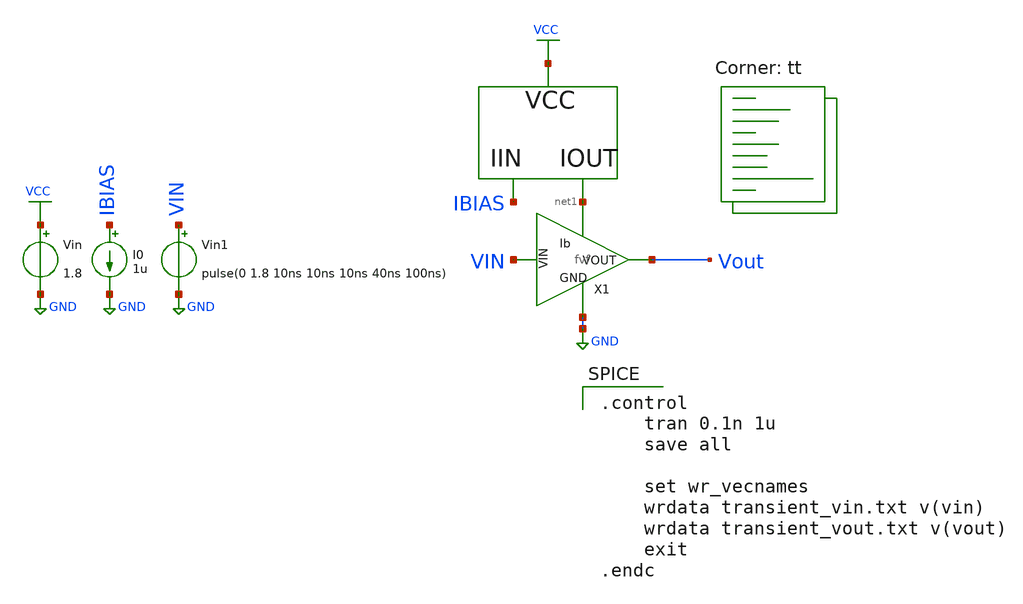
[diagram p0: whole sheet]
** sch_path: xschem/fvf_tb_tran.sch
**.subckt fvf_tb_tran
Vin VCC GND 1.8
I0 IBIAS GND 1u
X1 net1 GND VIN Vout fvf
Vin1 VIN GND pulse(0 1.8 10ns 10ns 10ns 40ns 100ns)
**** begin user architecture code
.lib $::SKYWATER_MODELS/sky130.lib.spice tt

.control
    tran 0.1n 1u
    save all

    set wr_vecnames
    wrdata transient_vin.txt v(vin)
    wrdata transient_vout.txt v(vout)
    exit
.endc

**** end user architecture code
**.ends

* expanding   symbol:  /foss/designs/fvf-chipathon-2024/xschem/fvf.sym # of pins=4
** sym_path: xschem/fvf.sym
** sch_path: xschem/fvf.sch
.subckt fvf Ib GND VIN VOUT
*.ipin VIN
*.opin VOUT
*.iopin GND
*.ipin Ib
XM1 Ib VIN VOUT GND sky130_fd_pr__nfet_01v8 L=1 W=15 nf=1 ad='int((nf+1)/2) * W/nf * 0.29' as='int((nf+2)/2) * W/nf * 0.29'
+ pd='2*int((nf+1)/2) * (W/nf + 0.29)' ps='2*int((nf+2)/2) * (W/nf + 0.29)' nrd='0.29 / W' nrs='0.29 / W'
+ sa=0 sb=0 sd=0 mult=1 m=1
XM2 VOUT Ib GND GND sky130_fd_pr__nfet_01v8 L=1 W=15 nf=1 ad='int((nf+1)/2) * W/nf * 0.29' as='int((nf+2)/2) * W/nf * 0.29'
+ pd='2*int((nf+1)/2) * (W/nf + 0.29)' ps='2*int((nf+2)/2) * (W/nf + 0.29)' nrd='0.29 / W' nrs='0.29 / W'
+ sa=0 sb=0 sd=0 mult=1 m=1
.ends

.GLOBAL GND
.GLOBAL VCC
.end
